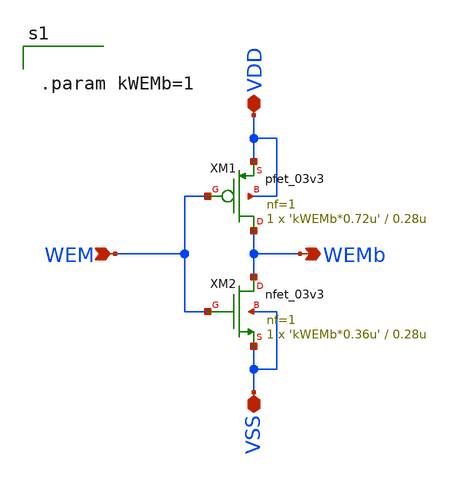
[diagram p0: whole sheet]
** sch_path: CAD3/wem_inverter.sch
**.subckt wem_inverter WEM WEMb VDD VSS
*.ipin WEM
*.opin WEMb
*.iopin VDD
*.iopin VSS
XM1 WEMb WEM VDD VDD pfet_03v3 L=0.28u W='kWEMb*0.72u' nf=1 ad='int((nf+1)/2) * W/nf * 0.18u' as='int((nf+2)/2) * W/nf * 0.18u'
+ pd='2*int((nf+1)/2) * (W/nf + 0.18u)' ps='2*int((nf+2)/2) * (W/nf + 0.18u)' nrd='0.18u / W' nrs='0.18u / W'
+ sa=0 sb=0 sd=0 m=1
XM2 WEMb WEM VSS VSS nfet_03v3 L=0.28u W='kWEMb*0.36u' nf=1 ad='int((nf+1)/2) * W/nf * 0.18u' as='int((nf+2)/2) * W/nf * 0.18u'
+ pd='2*int((nf+1)/2) * (W/nf + 0.18u)' ps='2*int((nf+2)/2) * (W/nf + 0.18u)' nrd='0.18u / W' nrs='0.18u / W'
+ sa=0 sb=0 sd=0 m=1
**** begin user architecture code


.param kWEMb=1


**** end user architecture code
**.ends
.end
